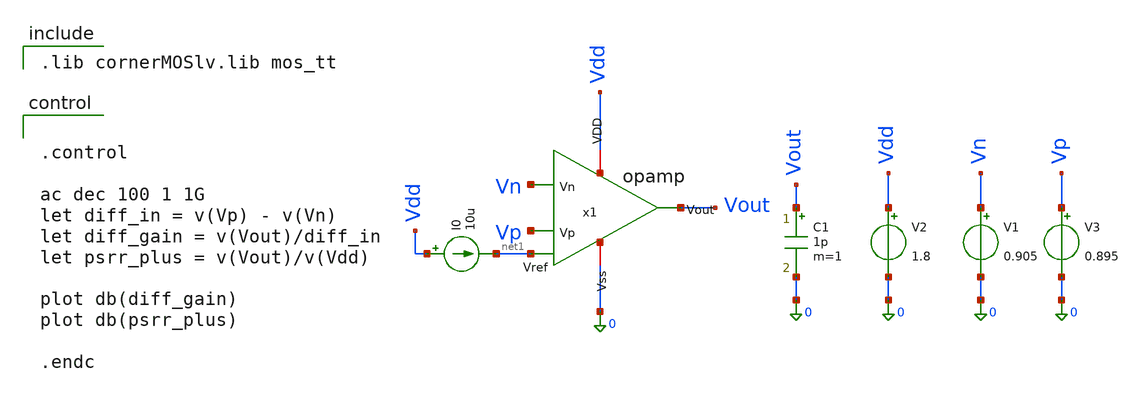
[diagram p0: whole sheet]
** sch_path: designs/opamp/testbench.sch
**.subckt testbench
V2 Vdd 0 1.8
V1 Vn 0 0.905
V3 Vp 0 0.895
I0 Vdd net1 10u
C1 Vout 0 1p m=1
x1 Vdd net1 Vn Vp Vout 0 opamp
**** begin user architecture code

.lib cornerMOSlv.lib mos_tt



.control

ac dec 100 1 1G
let diff_in = v(Vp) - v(Vn)
let diff_gain = v(Vout)/diff_in
let psrr_plus = v(Vout)/v(Vdd)

plot db(diff_gain)
plot db(psrr_plus)

.endc


**** end user architecture code
**.ends

* expanding   symbol:
*+  /var/home/bleroux/Documents/stage_IEMN/analog-asic-design/designs/opamp/opamp.sym # of pins=6
** sym_path: designs/opamp/opamp.sym
** sch_path: designs/opamp/opamp.sch
.subckt opamp VDD Vref Vn Vp Vout Vss
*.ipin Vn
*.ipin Vp
*.opin Vout
*.iopin VDD
*.iopin Vref
*.iopin Vss
**** begin user architecture code

.lib cornerMOSlv.lib mos_tt

**** end user architecture code
XM3 net2 Vn net1 net1 sg13_lv_nmos w=0.15u l=0.13u ng=1 m=1 mm_ok=1
XM4 net3 Vp net1 net1 sg13_lv_nmos w=0.15u l=0.13u ng=1 m=1 mm_ok=1
XM5 net2 net2 VDD VDD sg13_lv_pmos w=0.15u l=0.13u ng=1 m=1 mm_ok=1
XM6 net3 net2 VDD VDD sg13_lv_pmos w=0.15u l=0.13u ng=1 m=1 mm_ok=1
XM7 net1 Vref Vss Vss sg13_lv_nmos w=0.15u l=0.13u ng=1 m=1 mm_ok=1
XM8 Vout Vref Vss Vss sg13_lv_nmos w=0.15u l=0.13u ng=1 m=1 mm_ok=1
XM9 Vref Vref Vss Vss sg13_lv_nmos w=0.15u l=0.13u ng=1 m=1 mm_ok=1
XM10 Vout net3 VDD VDD sg13_lv_pmos w=0.15u l=0.13u ng=1 m=1 mm_ok=1
C1 Vout net3 10p m=1
.ends

.end
